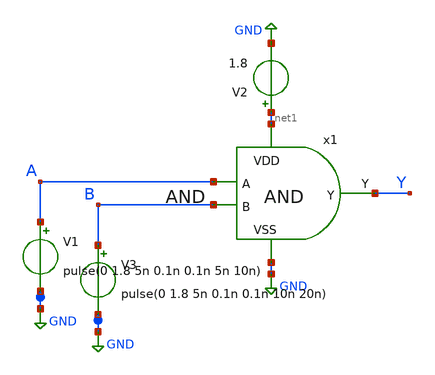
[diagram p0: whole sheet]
** sch_path: Layouts and Schematics/Spice Sim and Schem/andtest.sch
**.subckt andtest
V1 A GND pulse(0 1.8 5n 0.1n 0.1n 5n 10n)
V2 net1 GND 1.8
V3 B GND pulse(0 1.8 5n 0.1n 0.1n 10n 20n)
x1 net1 A Y B GND and
**** begin user architecture code
 .lib $::SKYWATER_MODELS/sky130.lib.spice tt

.include /home/wyatt/EE431
.tran 1n 40n
.control
run
.endc

**** end user architecture code
**.ends

* expanding   symbol:  and.sym # of pins=5
** sym_path: Layouts and Schematics/Spice Sim and Schem/and.sym
** sch_path: Layouts and Schematics/Spice Sim and Schem/and.sch
.subckt and VDD A Y B VSS
*.opin Y
*.ipin VSS
*.ipin VDD
*.ipin A
*.ipin B
x1 VDD net1 Y VSS inv
x2 VDD A net1 B VSS nand
.ends


* expanding   symbol:  inv.sym # of pins=4
** sym_path: Layouts and Schematics/Spice Sim and Schem/inv.sym
** sch_path: Layouts and Schematics/Spice Sim and Schem/inv.sch
.subckt inv VDD X Y GND
*.ipin X
*.iopin VDD
*.iopin GND
*.opin Y
XM1 Y X GND GND sky130_fd_pr__nfet_01v8 L=0.5 W=1 nf=1 ad='int((nf+1)/2) * W/nf * 0.29' as='int((nf+2)/2) * W/nf * 0.29'
+ pd='2*int((nf+1)/2) * (W/nf + 0.29)' ps='2*int((nf+2)/2) * (W/nf + 0.29)' nrd='0.29 / W' nrs='0.29 / W'
+ sa=0 sb=0 sd=0 mult=1 m=1
XM2 Y X VDD VDD sky130_fd_pr__pfet_01v8 L=0.5 W=2 nf=1 ad='int((nf+1)/2) * W/nf * 0.29' as='int((nf+2)/2) * W/nf * 0.29'
+ pd='2*int((nf+1)/2) * (W/nf + 0.29)' ps='2*int((nf+2)/2) * (W/nf + 0.29)' nrd='0.29 / W' nrs='0.29 / W'
+ sa=0 sb=0 sd=0 mult=1 m=1
.ends


* expanding   symbol:  nand.sym # of pins=5
** sym_path: Layouts and Schematics/Spice Sim and Schem/nand.sym
** sch_path: Layouts and Schematics/Spice Sim and Schem/nand.sch
.subckt nand VDD A Y B VSS
*.ipin A
*.ipin B
*.ipin VSS
*.opin Y
*.ipin VDD
XM1 Y B net1 VSS sky130_fd_pr__nfet_01v8 L=0.5 W=2 nf=1 ad='int((nf+1)/2) * W/nf * 0.29' as='int((nf+2)/2) * W/nf * 0.29'
+ pd='2*int((nf+1)/2) * (W/nf + 0.29)' ps='2*int((nf+2)/2) * (W/nf + 0.29)' nrd='0.29 / W' nrs='0.29 / W'
+ sa=0 sb=0 sd=0 mult=1 m=1
XM3 Y B VDD VDD sky130_fd_pr__pfet_01v8 L=0.5 W=2 nf=1 ad='int((nf+1)/2) * W/nf * 0.29' as='int((nf+2)/2) * W/nf * 0.29'
+ pd='2*int((nf+1)/2) * (W/nf + 0.29)' ps='2*int((nf+2)/2) * (W/nf + 0.29)' nrd='0.29 / W' nrs='0.29 / W'
+ sa=0 sb=0 sd=0 mult=1 m=1
XM4 Y A VDD VDD sky130_fd_pr__pfet_01v8 L=0.5 W=2 nf=1 ad='int((nf+1)/2) * W/nf * 0.29' as='int((nf+2)/2) * W/nf * 0.29'
+ pd='2*int((nf+1)/2) * (W/nf + 0.29)' ps='2*int((nf+2)/2) * (W/nf + 0.29)' nrd='0.29 / W' nrs='0.29 / W'
+ sa=0 sb=0 sd=0 mult=1 m=1
XM2 net1 A VSS VSS sky130_fd_pr__nfet_01v8 L=0.5 W=2 nf=1 ad='int((nf+1)/2) * W/nf * 0.29' as='int((nf+2)/2) * W/nf * 0.29'
+ pd='2*int((nf+1)/2) * (W/nf + 0.29)' ps='2*int((nf+2)/2) * (W/nf + 0.29)' nrd='0.29 / W' nrs='0.29 / W'
+ sa=0 sb=0 sd=0 mult=1 m=1
.ends

.GLOBAL GND
.end
